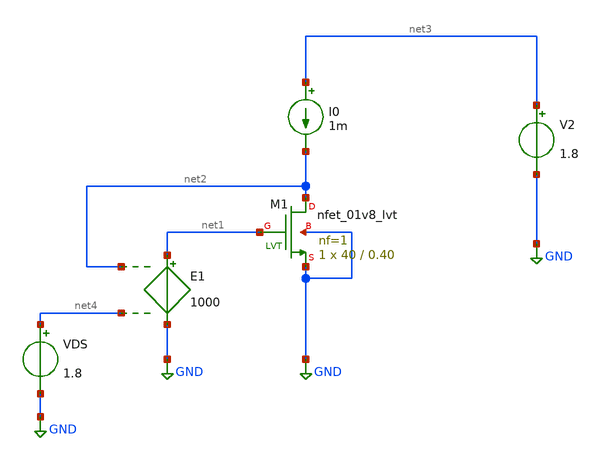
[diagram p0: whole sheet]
** sch_path: Simple-CS-Amplifier/csamp1.sch
**.subckt csamp1
XM1 net2 net1 GND GND sky130_fd_pr__nfet_01v8_lvt L=0.40 W=40 nf=1 ad='int((nf+1)/2) * W/nf * 0.29' as='int((nf+2)/2) * W/nf * 0.29'
+ pd='2*int((nf+1)/2) * (W/nf + 0.29)' ps='2*int((nf+2)/2) * (W/nf + 0.29)' nrd='0.29 / W' nrs='0.29 / W'
+ sa=0 sb=0 sd=0 mult=1 m=1
E1 net1 GND net2 net4 1000
I0 net3 net2 1m
VDS net4 GND 1.8
V2 net3 GND 1.8
**** begin user architecture code



.lib /usr/local/share/pdk/sky130A/libs.tech/ngspice/sky130.lib.spice tt
.option wnflag=1 scale=1e-6

.control
save all
save @m.xm1.msky130_fd_pr__nfet_01v8_lvt[vgs]
save @m.xm1.msky130_fd_pr__nfet_01v8_lvt[vds]
save @m.xm1.msky130_fd_pr__nfet_01v8_lvt[gm]
save @m.xm1.msky130_fd_pr__nfet_01v8_lvt[gds]

dc VDS 0.2 1.8 1m

let vgs = @m.xm1.msky130_fd_pr__nfet_01v8_lvt[vgs]
let vds = @m.xm1.msky130_fd_pr__nfet_01v8_lvt[vds]
let gm = @m.xm1.msky130_fd_pr__nfet_01v8_lvt[gm]
let gds = @m.xm1.msky130_fd_pr__nfet_01v8_lvt[gds]
let ro = 1/gds

let gain = gm*ro

let ao = -1/(deriv(vgs))

plot ao
.endc


**** end user architecture code
**.ends
.GLOBAL GND
.end
